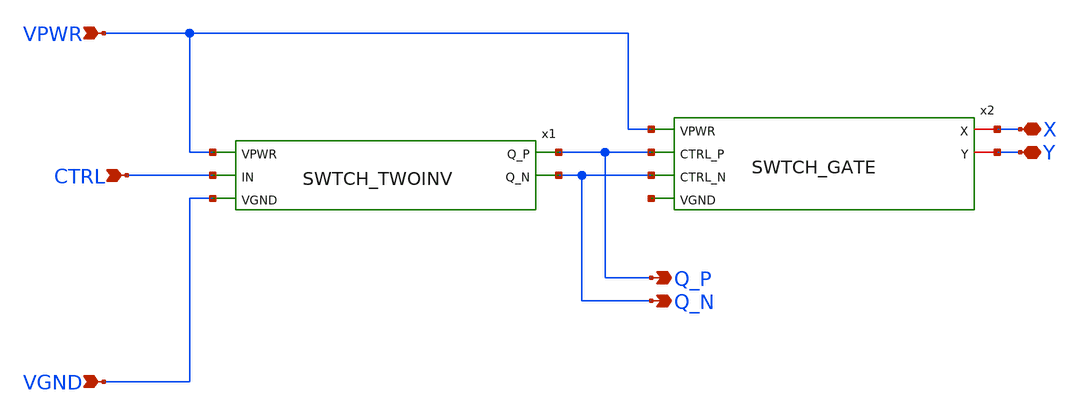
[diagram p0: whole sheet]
** sch_path: swtch_unit2_sky130nm/design/SWTCH_UNIT2_SKY130NM/SWTCH_UNIT2.sch
**.subckt SWTCH_UNIT2 VPWR VGND CTRL X Y Q_P Q_N
*.ipin VPWR
*.ipin VGND
*.ipin CTRL
*.iopin X
*.iopin Y
*.opin Q_P
*.opin Q_N
x1 VPWR CTRL Q_P Q_N VGND SWTCH_TWOINV
x2 VPWR X Q_P Q_N Y net1 SWTCH_GATE
**.ends

* expanding   symbol:
*+  /home/couch/dev/personal/chacha-silicon/tt09-analog-switch/swtch_twoinv_sky130nm/design/SWTCH_TWOINV_SKY130NM/SWTCH_TWOINV.sym # of pins=5
** sym_path: swtch_twoinv_sky130nm/design/SWTCH_TWOINV_SKY130NM/SWTCH_TWOINV.sym
** sch_path: swtch_twoinv_sky130nm/design/SWTCH_TWOINV_SKY130NM/SWTCH_TWOINV.sch
.subckt SWTCH_TWOINV VPWR IN Q_P Q_N VGND
*.ipin VPWR
*.ipin VGND
*.ipin IN
*.opin Q_P
*.opin Q_N
XM1 Q_N IN VPWR VPWR sky130_fd_pr__pfet_01v8 L=0.15 W=3 nf=2 ad='int((nf+1)/2) * W/nf * 0.29' as='int((nf+2)/2) * W/nf * 0.29'
+ pd='2*int((nf+1)/2) * (W/nf + 0.29)' ps='2*int((nf+2)/2) * (W/nf + 0.29)' nrd='0.29 / W' nrs='0.29 / W'
+ sa=0 sb=0 sd=0 mult=1 m=1
XM2 Q_N IN VGND VGND sky130_fd_pr__nfet_01v8 L=0.15 W=1.5 nf=1 ad='int((nf+1)/2) * W/nf * 0.29' as='int((nf+2)/2) * W/nf * 0.29'
+ pd='2*int((nf+1)/2) * (W/nf + 0.29)' ps='2*int((nf+2)/2) * (W/nf + 0.29)' nrd='0.29 / W' nrs='0.29 / W'
+ sa=0 sb=0 sd=0 mult=1 m=1
XM3 Q_P Q_N VPWR VPWR sky130_fd_pr__pfet_01v8 L=0.15 W=3 nf=2 ad='int((nf+1)/2) * W/nf * 0.29' as='int((nf+2)/2) * W/nf * 0.29'
+ pd='2*int((nf+1)/2) * (W/nf + 0.29)' ps='2*int((nf+2)/2) * (W/nf + 0.29)' nrd='0.29 / W' nrs='0.29 / W'
+ sa=0 sb=0 sd=0 mult=1 m=1
XM4 Q_P Q_N VGND VGND sky130_fd_pr__nfet_01v8 L=0.15 W=1.5 nf=1 ad='int((nf+1)/2) * W/nf * 0.29' as='int((nf+2)/2) * W/nf * 0.29'
+ pd='2*int((nf+1)/2) * (W/nf + 0.29)' ps='2*int((nf+2)/2) * (W/nf + 0.29)' nrd='0.29 / W' nrs='0.29 / W'
+ sa=0 sb=0 sd=0 mult=1 m=1
.ends


* expanding   symbol:
*+  /home/couch/dev/personal/chacha-silicon/tt09-analog-switch/swtch_gate_sky130nm/design/SWTCH_GATE_SKY130NM/SWTCH_GATE.sym # of pins=6
** sym_path: swtch_gate_sky130nm/design/SWTCH_GATE_SKY130NM/SWTCH_GATE.sym
** sch_path: swtch_gate_sky130nm/design/SWTCH_GATE_SKY130NM/SWTCH_GATE.sch
.subckt SWTCH_GATE VPWR X CTRL_P CTRL_N Y VGND
*.ipin VPWR
*.ipin VGND
*.ipin CTRL_P
*.ipin CTRL_N
*.iopin X
*.iopin Y
XM3 Y CTRL_N X VPWR sky130_fd_pr__pfet_01v8_lvt L=0.35 W=94.5 nf=21 ad='int((nf+1)/2) * W/nf * 0.29'
+ as='int((nf+2)/2) * W/nf * 0.29' pd='2*int((nf+1)/2) * (W/nf + 0.29)' ps='2*int((nf+2)/2) * (W/nf + 0.29)'
+ nrd='0.29 / W' nrs='0.29 / W' sa=0 sb=0 sd=0 mult=1 m=1
XM4 X CTRL_P Y VGND sky130_fd_pr__nfet_01v8_lvt L=0.15 W=31.5 nf=7 ad='int((nf+1)/2) * W/nf * 0.29' as='int((nf+2)/2) * W/nf * 0.29'
+ pd='2*int((nf+1)/2) * (W/nf + 0.29)' ps='2*int((nf+2)/2) * (W/nf + 0.29)' nrd='0.29 / W' nrs='0.29 / W'
+ sa=0 sb=0 sd=0 mult=1 m=1
.ends

.end
